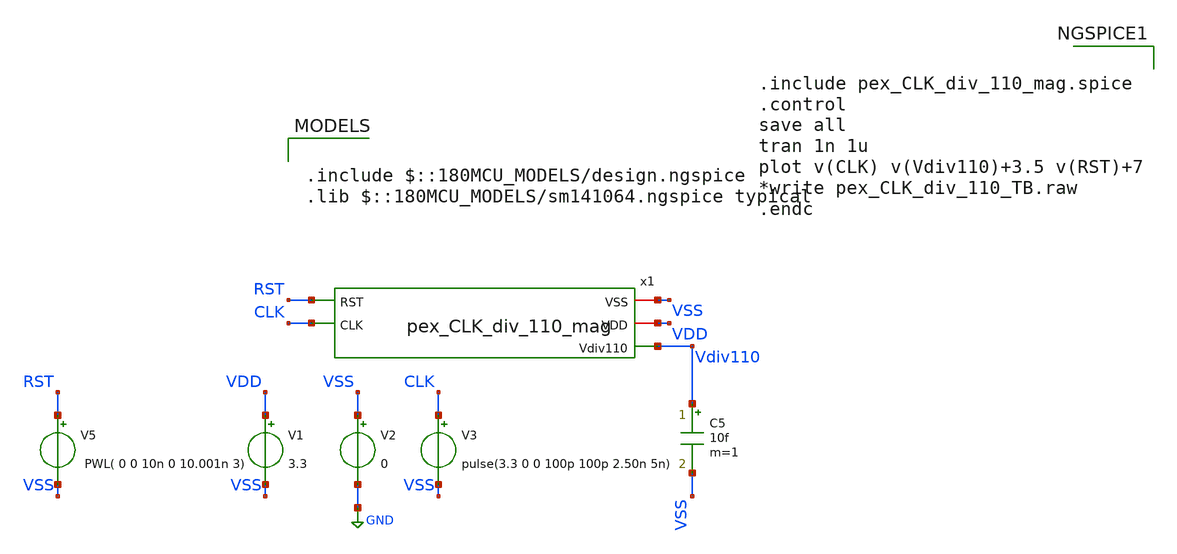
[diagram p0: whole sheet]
** sch_path: Clock_Generator_PAKISTAN_02/Schematics/pex_CLK_div_110_TB.sch
**.subckt pex_CLK_div_110_TB
V1 VDD VSS 3.3
V2 VSS GND 0
V3 CLK VSS pulse(3.3 0 0 100p 100p 2.50n 5n)
C5 Vdiv110 VSS 10f m=1
V5 RST VSS PWL( 0 0 10n 0 10.001n 3)
x1 VSS VDD RST Vdiv110 CLK pex_CLK_div_110_mag
**** begin user architecture code

.include $::180MCU_MODELS/design.ngspice
.lib $::180MCU_MODELS/sm141064.ngspice typical



.include pex_CLK_div_110_mag.spice
.control
save all
tran 1n 1u
plot v(CLK) v(Vdiv110)+3.5 v(RST)+7
*write pex_CLK_div_110_TB.raw
.endc


**** end user architecture code
**.ends
.GLOBAL GND
.end
